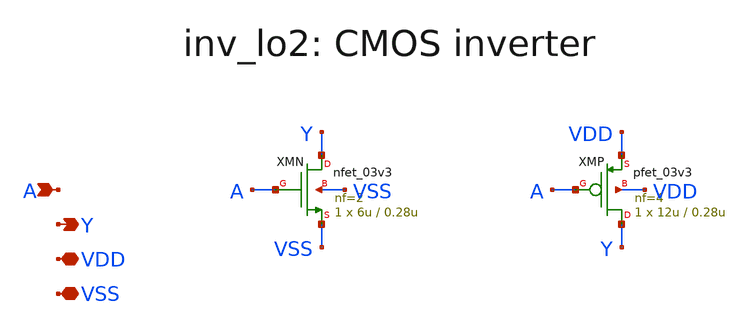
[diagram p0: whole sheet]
** sch_path: v1_claude/xschem/inv_lo2.sch
**.subckt inv_lo2 A Y VDD VSS
*.ipin A
*.opin Y
*.iopin VDD
*.iopin VSS
XMN Y A VSS VSS nfet_03v3 L=0.28u W=6u nf=2 ad='int((nf+1)/2) * W/nf * 0.18u' as='int((nf+2)/2) * W/nf * 0.18u'
+ pd='2*int((nf+1)/2) * (W/nf + 0.18u)' ps='2*int((nf+2)/2) * (W/nf + 0.18u)' nrd='0.18u / W' nrs='0.18u / W'
+ sa=0 sb=0 sd=0 m=1
XMP Y A VDD VDD pfet_03v3 L=0.28u W=12u nf=4 ad='int((nf+1)/2) * W/nf * 0.18u' as='int((nf+2)/2) * W/nf * 0.18u'
+ pd='2*int((nf+1)/2) * (W/nf + 0.18u)' ps='2*int((nf+2)/2) * (W/nf + 0.18u)' nrd='0.18u / W' nrs='0.18u / W'
+ sa=0 sb=0 sd=0 m=1
**.ends
.end
